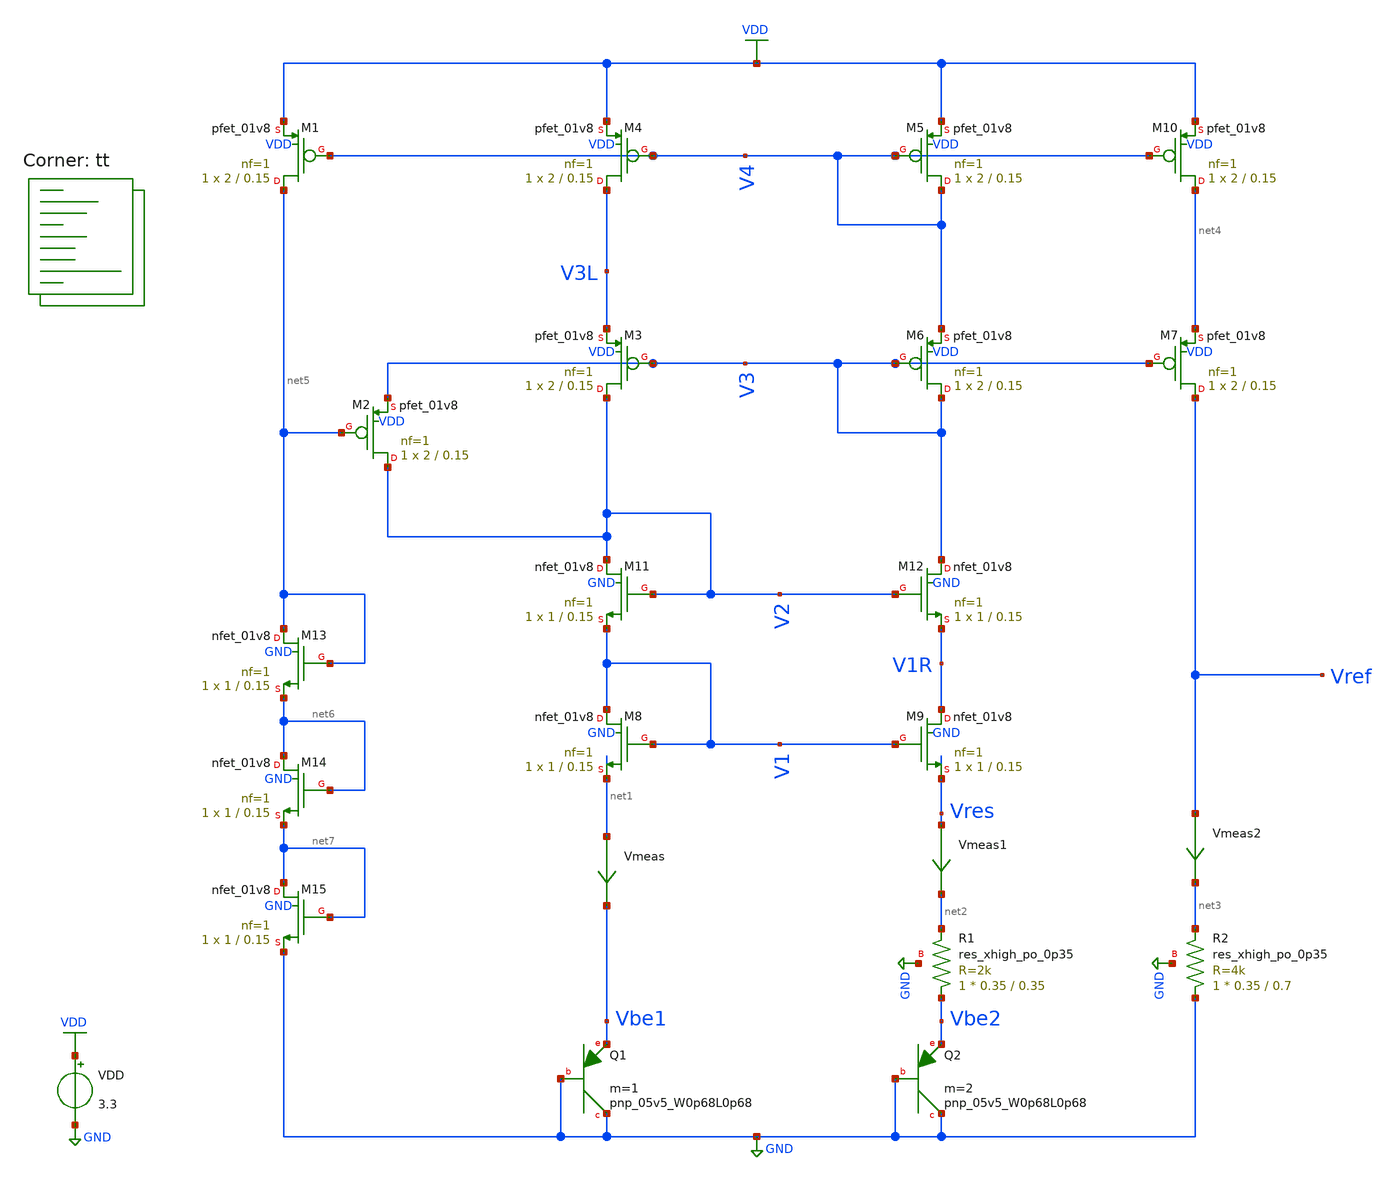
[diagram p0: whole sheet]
** sch_path: projects/pll/bandgapref/xschem_ngspice/mos_bandgap_baker2.sch
**.subckt mos_bandgap_baker2
XM4 V3L V4 VDD VDD sky130_fd_pr__pfet_01v8 L=0.15 W=2 nf=1 ad='int((nf+1)/2) * W/nf * 0.29' as='int((nf+2)/2) * W/nf * 0.29'
+ pd='2*int((nf+1)/2) * (W/nf + 0.29)' ps='2*int((nf+2)/2) * (W/nf + 0.29)' nrd='0.29 / W' nrs='0.29 / W'
+ sa=0 sb=0 sd=0 mult=1 m=1
XM5 V4 V4 VDD VDD sky130_fd_pr__pfet_01v8 L=0.15 W=2 nf=1 ad='int((nf+1)/2) * W/nf * 0.29' as='int((nf+2)/2) * W/nf * 0.29'
+ pd='2*int((nf+1)/2) * (W/nf + 0.29)' ps='2*int((nf+2)/2) * (W/nf + 0.29)' nrd='0.29 / W' nrs='0.29 / W'
+ sa=0 sb=0 sd=0 mult=1 m=1
VDD VDD GND 3.3
Vmeas net1 Vbe1 0
.save i(vmeas)
Vmeas1 Vres net2 0
.save i(vmeas1)
XR1 Vbe2 net2 GND sky130_fd_pr__res_xhigh_po_0p35 L=0.35 mult=1 m=1
XQ1 GND GND Vbe1 sky130_fd_pr__pnp_05v5_W0p68L0p68 m=1
XQ2 GND GND Vbe2 sky130_fd_pr__pnp_05v5_W0p68L0p68 m=2
XM8 V1 V1 net1 GND sky130_fd_pr__nfet_01v8 L=0.15 W=1 nf=1 ad='int((nf+1)/2) * W/nf * 0.29' as='int((nf+2)/2) * W/nf * 0.29'
+ pd='2*int((nf+1)/2) * (W/nf + 0.29)' ps='2*int((nf+2)/2) * (W/nf + 0.29)' nrd='0.29 / W' nrs='0.29 / W'
+ sa=0 sb=0 sd=0 mult=1 m=1
XM9 V1R V1 Vres GND sky130_fd_pr__nfet_01v8 L=0.15 W=1 nf=1 ad='int((nf+1)/2) * W/nf * 0.29' as='int((nf+2)/2) * W/nf * 0.29'
+ pd='2*int((nf+1)/2) * (W/nf + 0.29)' ps='2*int((nf+2)/2) * (W/nf + 0.29)' nrd='0.29 / W' nrs='0.29 / W'
+ sa=0 sb=0 sd=0 mult=1 m=1
XM10 net4 V4 VDD VDD sky130_fd_pr__pfet_01v8 L=0.15 W=2 nf=1 ad='int((nf+1)/2) * W/nf * 0.29' as='int((nf+2)/2) * W/nf * 0.29'
+ pd='2*int((nf+1)/2) * (W/nf + 0.29)' ps='2*int((nf+2)/2) * (W/nf + 0.29)' nrd='0.29 / W' nrs='0.29 / W'
+ sa=0 sb=0 sd=0 mult=1 m=1
Vmeas2 Vref net3 0
.save i(vmeas2)
XR2 GND net3 GND sky130_fd_pr__res_xhigh_po_0p35 L=0.7 mult=1 m=1
XM1 net5 V4 VDD VDD sky130_fd_pr__pfet_01v8 L=0.15 W=2 nf=1 ad='int((nf+1)/2) * W/nf * 0.29' as='int((nf+2)/2) * W/nf * 0.29'
+ pd='2*int((nf+1)/2) * (W/nf + 0.29)' ps='2*int((nf+2)/2) * (W/nf + 0.29)' nrd='0.29 / W' nrs='0.29 / W'
+ sa=0 sb=0 sd=0 mult=1 m=1
XM2 V2 net5 V3 VDD sky130_fd_pr__pfet_01v8 L=0.15 W=2 nf=1 ad='int((nf+1)/2) * W/nf * 0.29' as='int((nf+2)/2) * W/nf * 0.29'
+ pd='2*int((nf+1)/2) * (W/nf + 0.29)' ps='2*int((nf+2)/2) * (W/nf + 0.29)' nrd='0.29 / W' nrs='0.29 / W'
+ sa=0 sb=0 sd=0 mult=1 m=1
XM3 V2 V3 V3L VDD sky130_fd_pr__pfet_01v8 L=0.15 W=2 nf=1 ad='int((nf+1)/2) * W/nf * 0.29' as='int((nf+2)/2) * W/nf * 0.29'
+ pd='2*int((nf+1)/2) * (W/nf + 0.29)' ps='2*int((nf+2)/2) * (W/nf + 0.29)' nrd='0.29 / W' nrs='0.29 / W'
+ sa=0 sb=0 sd=0 mult=1 m=1
XM6 V3 V3 V4 VDD sky130_fd_pr__pfet_01v8 L=0.15 W=2 nf=1 ad='int((nf+1)/2) * W/nf * 0.29' as='int((nf+2)/2) * W/nf * 0.29'
+ pd='2*int((nf+1)/2) * (W/nf + 0.29)' ps='2*int((nf+2)/2) * (W/nf + 0.29)' nrd='0.29 / W' nrs='0.29 / W'
+ sa=0 sb=0 sd=0 mult=1 m=1
XM7 Vref V3 net4 VDD sky130_fd_pr__pfet_01v8 L=0.15 W=2 nf=1 ad='int((nf+1)/2) * W/nf * 0.29' as='int((nf+2)/2) * W/nf * 0.29'
+ pd='2*int((nf+1)/2) * (W/nf + 0.29)' ps='2*int((nf+2)/2) * (W/nf + 0.29)' nrd='0.29 / W' nrs='0.29 / W'
+ sa=0 sb=0 sd=0 mult=1 m=1
XM11 V2 V2 V1 GND sky130_fd_pr__nfet_01v8 L=0.15 W=1 nf=1 ad='int((nf+1)/2) * W/nf * 0.29' as='int((nf+2)/2) * W/nf * 0.29'
+ pd='2*int((nf+1)/2) * (W/nf + 0.29)' ps='2*int((nf+2)/2) * (W/nf + 0.29)' nrd='0.29 / W' nrs='0.29 / W'
+ sa=0 sb=0 sd=0 mult=1 m=1
XM12 V3 V2 V1R GND sky130_fd_pr__nfet_01v8 L=0.15 W=1 nf=1 ad='int((nf+1)/2) * W/nf * 0.29' as='int((nf+2)/2) * W/nf * 0.29'
+ pd='2*int((nf+1)/2) * (W/nf + 0.29)' ps='2*int((nf+2)/2) * (W/nf + 0.29)' nrd='0.29 / W' nrs='0.29 / W'
+ sa=0 sb=0 sd=0 mult=1 m=1
XM13 net5 net5 net6 GND sky130_fd_pr__nfet_01v8 L=0.15 W=1 nf=1 ad='int((nf+1)/2) * W/nf * 0.29' as='int((nf+2)/2) * W/nf * 0.29'
+ pd='2*int((nf+1)/2) * (W/nf + 0.29)' ps='2*int((nf+2)/2) * (W/nf + 0.29)' nrd='0.29 / W' nrs='0.29 / W'
+ sa=0 sb=0 sd=0 mult=1 m=1
XM14 net6 net6 net7 GND sky130_fd_pr__nfet_01v8 L=0.15 W=1 nf=1 ad='int((nf+1)/2) * W/nf * 0.29' as='int((nf+2)/2) * W/nf * 0.29'
+ pd='2*int((nf+1)/2) * (W/nf + 0.29)' ps='2*int((nf+2)/2) * (W/nf + 0.29)' nrd='0.29 / W' nrs='0.29 / W'
+ sa=0 sb=0 sd=0 mult=1 m=1
XM15 net7 net7 GND GND sky130_fd_pr__nfet_01v8 L=0.15 W=1 nf=1 ad='int((nf+1)/2) * W/nf * 0.29' as='int((nf+2)/2) * W/nf * 0.29'
+ pd='2*int((nf+1)/2) * (W/nf + 0.29)' ps='2*int((nf+2)/2) * (W/nf + 0.29)' nrd='0.29 / W' nrs='0.29 / W'
+ sa=0 sb=0 sd=0 mult=1 m=1
**** begin user architecture code
.lib $::SKYWATER_MODELS/sky130.lib.spice tt



.option method=gear
.option wnflag=1
.option savecurrents

.save @m.xm1.msky130_fd_pr__nfet_01v8[gm] @m.xm2.msky130_fd_pr__pfet_01v8[gm] @m.xm3.msky130_fd_pr__pfet_01v8[gm] @m.xm4.msky130_fd_pr__pfet_01v8[gm] @m.xm5.msky130_fd_pr__pfet_01v8[gm] @m.xm6.msky130_fd_pr__pfet_01v8[gm] @m.xm7.msky130_fd_pr__nfet_01v8[gm] @m.xm8.msky130_fd_pr__nfet_01v8[gm] @m.xm9.msky130_fd_pr__nfet_01v8[gm] @m.xm10.msky130_fd_pr__pfet_01v8[gm]

.control
save all
op
dc VDD 0 3.3 0.1 temp 0 100 1
* tran 4ns 40us
remzerovec
write mos_bandgap_baker2.raw
set appendwrite
.endc



**** end user architecture code
**.ends
.GLOBAL VDD
.GLOBAL GND
.end
